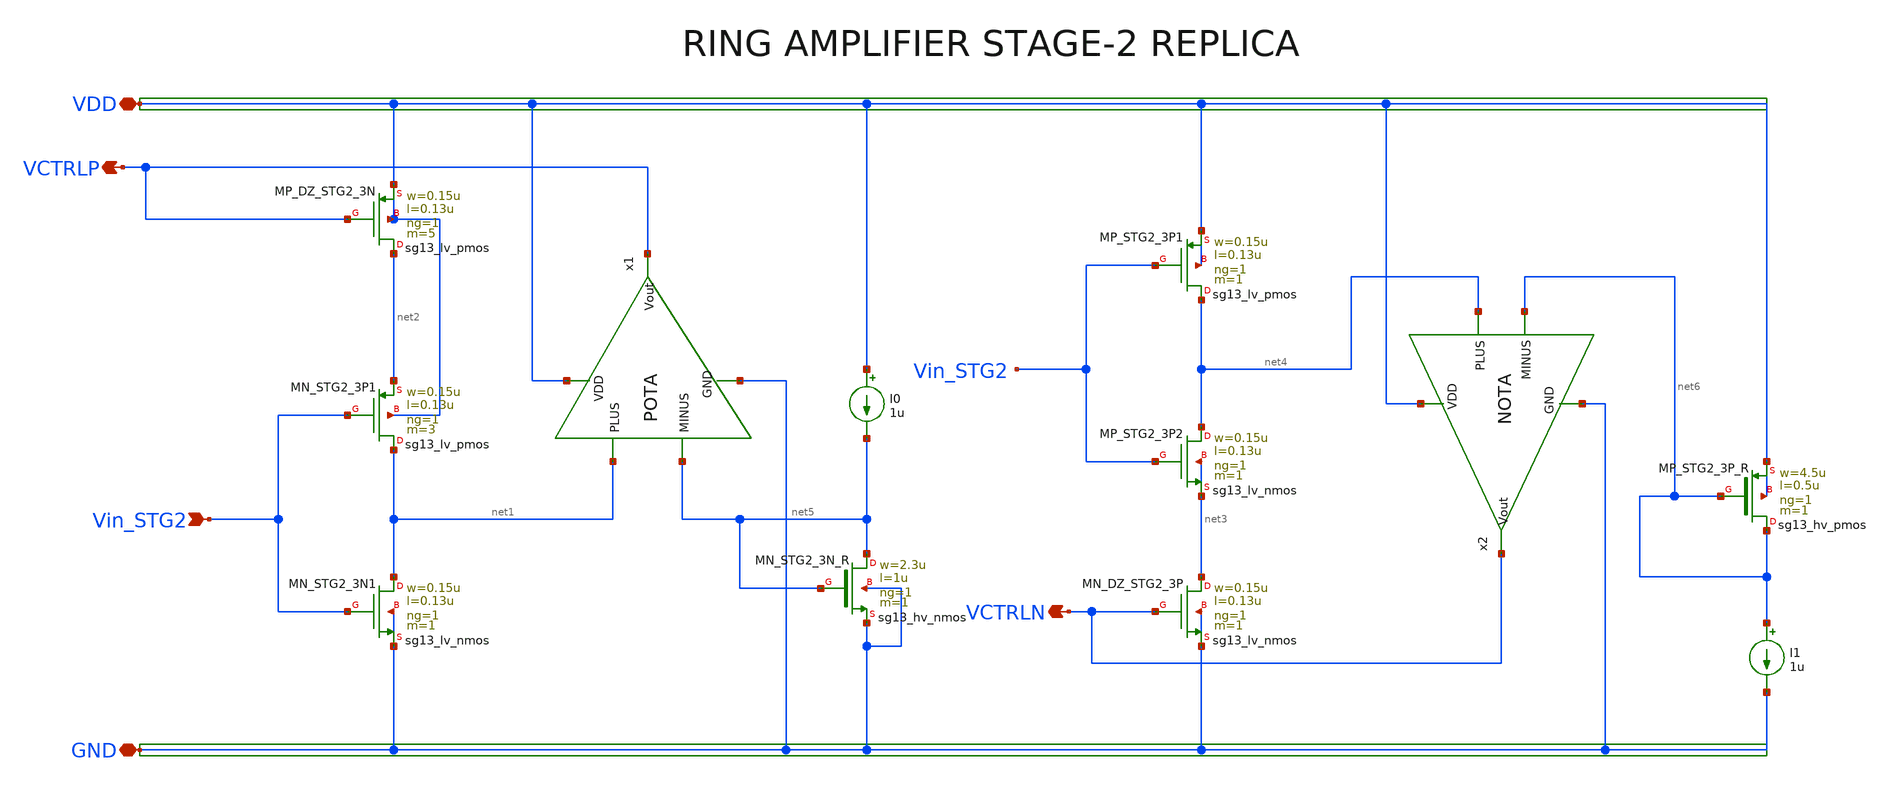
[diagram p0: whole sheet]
** sch_path: Design Files/RAMP/Fully-Diff-RAMP/STG2_Replica.sch
**.subckt STG2_Replica Vin_STG2 VDD GND VCTRLP VCTRLN
*.ipin Vin_STG2
*.iopin VDD
*.iopin GND
*.opin VCTRLP
*.opin VCTRLN
XMN_STG2_3N1 net1 Vin_STG2 GND GND sg13_lv_nmos w=0.15u l=0.13u ng=1 m=1 mm_ok=1
XMN_STG2_3P1 net1 Vin_STG2 net2 VDD sg13_lv_pmos w=0.15u l=0.13u ng=1 m=3 mm_ok=1
XMP_DZ_STG2_3N net2 VCTRLP VDD VDD sg13_lv_pmos w=0.15u l=0.13u ng=1 m=5 mm_ok=1
XMP_STG2_3P2 net4 Vin_STG2 net3 net3 sg13_lv_nmos w=0.15u l=0.13u ng=1 m=1 mm_ok=1
XMP_STG2_3P1 net4 Vin_STG2 VDD VDD sg13_lv_pmos w=0.15u l=0.13u ng=1 m=1 mm_ok=1
XMN_DZ_STG2_3P net3 VCTRLN GND GND sg13_lv_nmos w=0.15u l=0.13u ng=1 m=1 mm_ok=1
XMN_STG2_3N_R net5 net5 GND GND sg13_hv_nmos w=2.3u l=1u ng=1 m=1 mm_ok=1
I0 VDD net5 1u
x1 VDD net1 net5 VCTRLP GND POTA
XMP_STG2_3P_R net6 net6 VDD VDD sg13_hv_pmos w=4.5u l=0.5u ng=1 m=1 mm_ok=1
I1 net6 GND 1u
x2 VDD VCTRLN net4 net6 GND NOTA
**.ends

* expanding   symbol:  /foss/designs/RAMP/OTA/POTA.sym # of pins=5
** sym_path: Design Files/RAMP/OTA/POTA.sym
** sch_path: Design Files/RAMP/OTA/POTA.sch
.subckt POTA VDD PLUS MINUS Vout GND
*.ipin VDD
*.ipin GND
*.ipin PLUS
*.ipin MINUS
*.opin Vout
XM2 net2 PLUS net1 VDD sg13_lv_pmos w=1.2u l=0.5u ng=1 m=2 mm_ok=1
XM3 Vout MINUS net1 VDD sg13_lv_pmos w=1.2u l=0.5u ng=1 m=2 mm_ok=1
XM4 Vout net2 GND GND sg13_hv_nmos w=0.5u l=2u ng=1 m=1 mm_ok=1
XM5 net2 net2 GND GND sg13_hv_nmos w=0.5u l=2u ng=1 m=1 mm_ok=1
I1 VDD net1 2u
.ends


* expanding   symbol:  /foss/designs/RAMP/OTA/NOTA.sym # of pins=5
** sym_path: Design Files/RAMP/OTA/NOTA.sym
** sch_path: Design Files/RAMP/OTA/NOTA.sch
.subckt NOTA VDD Vout PLUS MINUS GND
*.ipin VDD
*.ipin GND
*.ipin PLUS
*.ipin MINUS
*.opin Vout
XM1 net2 PLUS net1 GND sg13_hv_nmos w=1.75u l=1u ng=1 m=2 mm_ok=1
XM2 Vout MINUS net1 GND sg13_hv_nmos w=1.75u l=1u ng=1 m=2 mm_ok=1
I0 net1 GND 2u
XM3 Vout net2 VDD VDD sg13_hv_pmos w=0.5u l=0.75u ng=1 m=1 mm_ok=1
XM4 net2 net2 VDD VDD sg13_hv_pmos w=0.5u l=0.75u ng=1 m=1 mm_ok=1
.ends

.GLOBAL GND
.end
